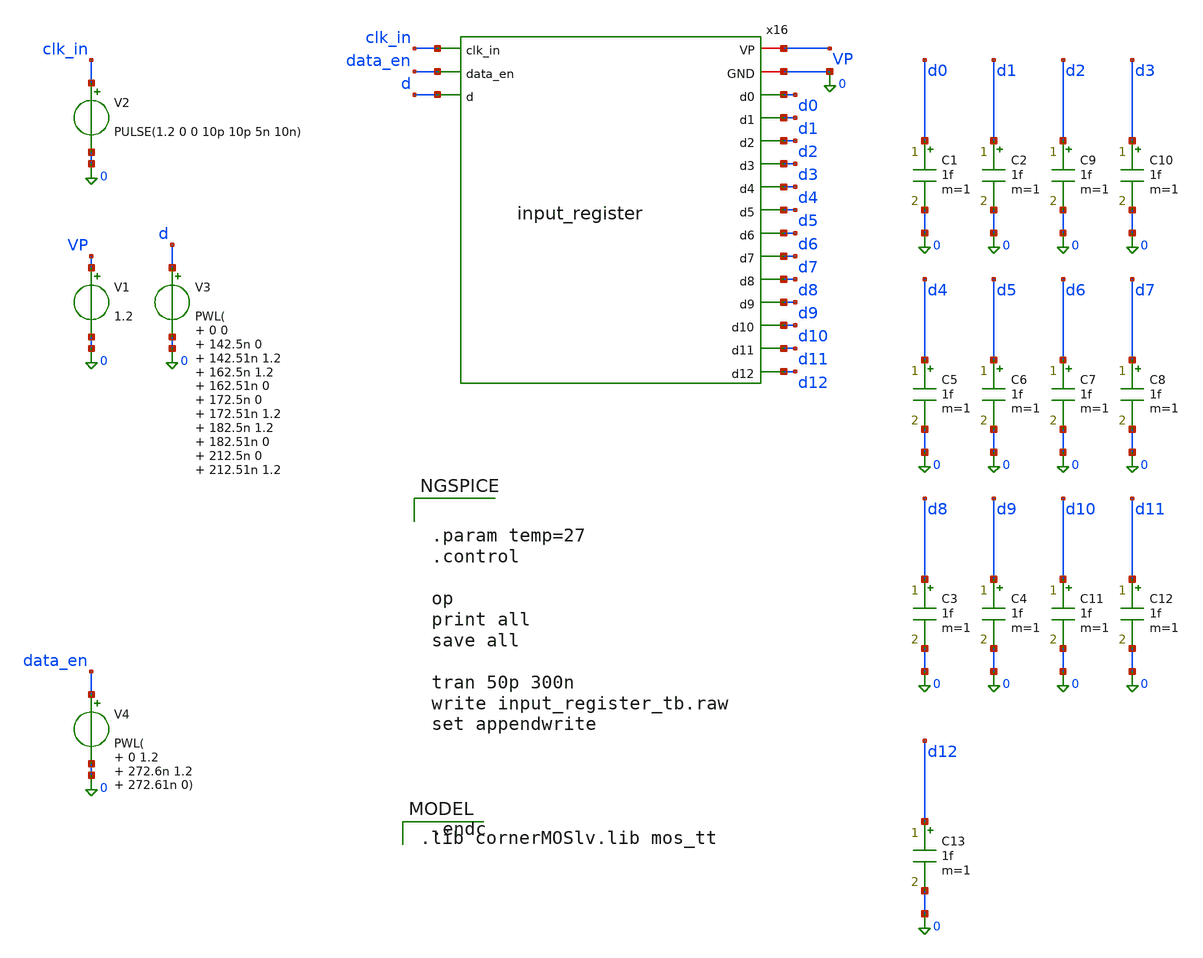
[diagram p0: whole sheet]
** sch_path: schematics/divider/tb/input_register_tb.sch
**.subckt input_register_tb
V1 VP 0 1.2
V2 clk_in 0 PULSE(1.2 0 0 10p 10p 5n 10n)
C1 d0 0 1f m=1
V3 d 0 PWL( 0 0 142.5n 0 142.51n 1.2 162.5n 1.2 162.51n 0 172.5n 0 172.51n 1.2 182.5n 1.2 182.51n 0
+ 212.5n 0 212.51n 1.2 222.5n 1.2 222.51n 0 232.5n 0 232.51n 1.2 242.5n 1.2 242.51n 0 262.5n 0 262.51n 1.2
+ 272.5n 1.2 272.51n 0)
C2 d1 0 1f m=1
C5 d4 0 1f m=1
C6 d5 0 1f m=1
C7 d6 0 1f m=1
C8 d7 0 1f m=1
C9 d2 0 1f m=1
C10 d3 0 1f m=1
V4 data_en 0 PWL( 0 1.2 272.6n 1.2 272.61n 0)
C3 d8 0 1f m=1
C4 d9 0 1f m=1
C11 d10 0 1f m=1
C12 d11 0 1f m=1
C13 d12 0 1f m=1
x16 VP 0 clk_in data_en d d0 d1 d2 d3 d4 d5 d6 d7 d8 d9 d10 d11 d12 input_register
**** begin user architecture code
 .lib cornerMOSlv.lib mos_tt



.param temp=27
.control

op
print all
save all

tran 50p 300n
write input_register_tb.raw
set appendwrite




.endc


**** end user architecture code
**.ends
.end
